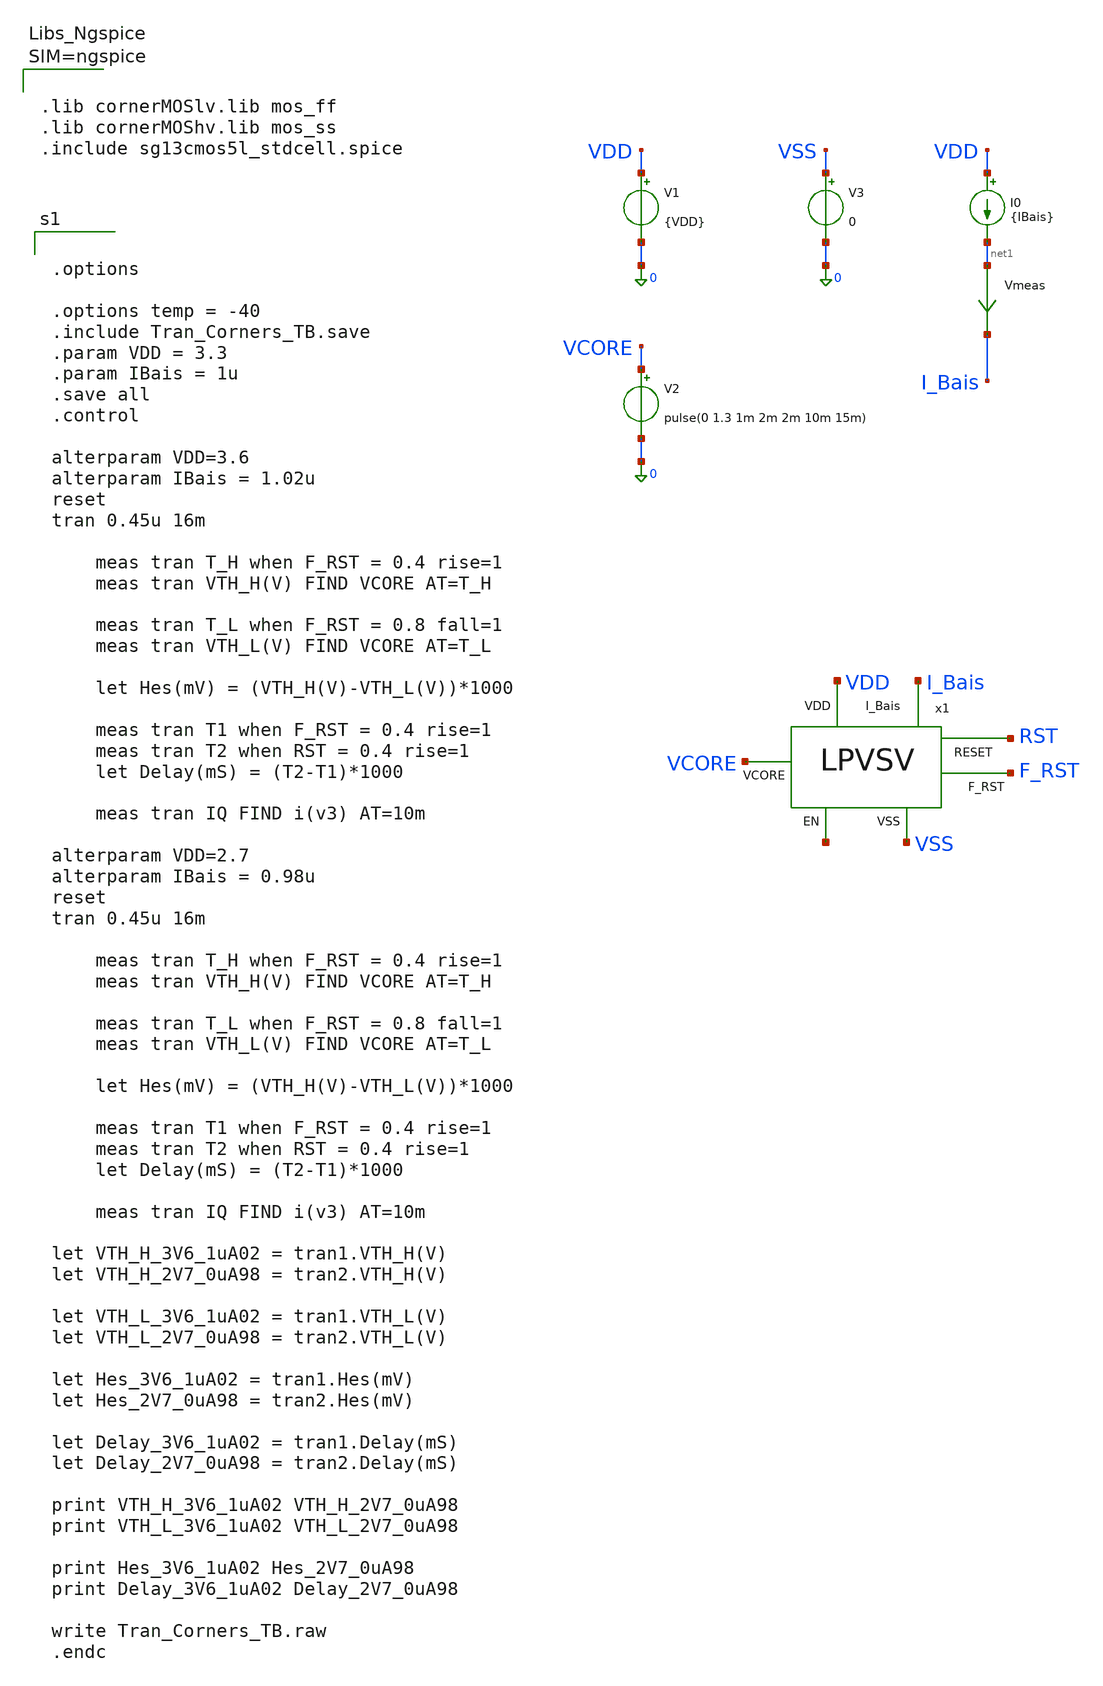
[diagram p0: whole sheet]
** sch_path: Simulation/Tran_Corners_TB.sch
**.subckt Tran_Corners_TB
I0 VDD net1 {IBais}
V1 VDD 0 {VDD}
V2 VCORE 0 pulse(0 1.3 1m 2m 2m 10m 15m)
V3 VSS 0 0
Vmeas net1 I_Bais 0
.save i(vmeas)
x1 VDD VCORE I_Bais RST F_RST VSS net2 LPVSV
**** begin user architecture code



.lib cornerMOSlv.lib mos_ff
.lib cornerMOShv.lib mos_ss
.include sg13cmos5l_stdcell.spice





.options

.options temp = -40
.include Tran_Corners_TB.save
.param VDD = 3.3
.param IBais = 1u
.save all
.control

alterparam VDD=3.6
alterparam IBais = 1.02u
reset
tran 0.45u 16m

	meas tran T_H when F_RST = 0.4 rise=1
	meas tran VTH_H(V) FIND VCORE AT=T_H

	meas tran T_L when F_RST = 0.8 fall=1
	meas tran VTH_L(V) FIND VCORE AT=T_L

	let Hes(mV) = (VTH_H(V)-VTH_L(V))*1000

	meas tran T1 when F_RST = 0.4 rise=1
	meas tran T2 when RST = 0.4 rise=1
	let Delay(mS) = (T2-T1)*1000

	meas tran IQ FIND i(v3) AT=10m

alterparam VDD=2.7
alterparam IBais = 0.98u
reset
tran 0.45u 16m

	meas tran T_H when F_RST = 0.4 rise=1
	meas tran VTH_H(V) FIND VCORE AT=T_H

	meas tran T_L when F_RST = 0.8 fall=1
	meas tran VTH_L(V) FIND VCORE AT=T_L

	let Hes(mV) = (VTH_H(V)-VTH_L(V))*1000

	meas tran T1 when F_RST = 0.4 rise=1
	meas tran T2 when RST = 0.4 rise=1
	let Delay(mS) = (T2-T1)*1000

	meas tran IQ FIND i(v3) AT=10m

let VTH_H_3V6_1uA02 = tran1.VTH_H(V)
let VTH_H_2V7_0uA98 = tran2.VTH_H(V)

let VTH_L_3V6_1uA02 = tran1.VTH_L(V)
let VTH_L_2V7_0uA98 = tran2.VTH_L(V)

let Hes_3V6_1uA02 = tran1.Hes(mV)
let Hes_2V7_0uA98 = tran2.Hes(mV)

let Delay_3V6_1uA02 = tran1.Delay(mS)
let Delay_2V7_0uA98 = tran2.Delay(mS)

print VTH_H_3V6_1uA02 VTH_H_2V7_0uA98
print VTH_L_3V6_1uA02 VTH_L_2V7_0uA98

print Hes_3V6_1uA02 Hes_2V7_0uA98
print Delay_3V6_1uA02 Delay_2V7_0uA98

write Tran_Corners_TB.raw
.endc


**** end user architecture code
**.ends
.end
